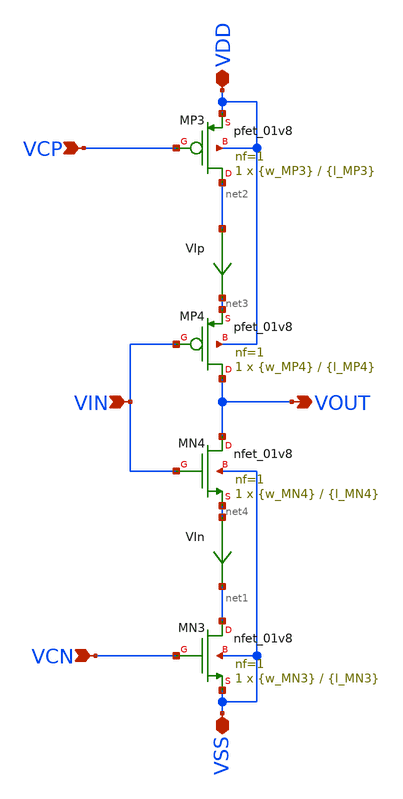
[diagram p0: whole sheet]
** sch_path: xschem/VCO/stage_starved.sch
**.subckt stage_starved VIN VOUT VDD VSS VCP VCN
*.ipin VIN
*.opin VOUT
*.iopin VDD
*.iopin VSS
*.ipin VCP
*.ipin VCN
XMP3 net2 VCP VDD VDD sky130_fd_pr__pfet_01v8 L={l_MP3} W={w_MP3} nf=1 ad='int((nf+1)/2) * W/nf * 0.29'
+ as='int((nf+2)/2) * W/nf * 0.29' pd='2*int((nf+1)/2) * (W/nf + 0.29)' ps='2*int((nf+2)/2) * (W/nf + 0.29)'
+ nrd='0.29 / W' nrs='0.29 / W' sa=0 sb=0 sd=0 mult=1 m=1
XMP4 VOUT VIN net3 VDD sky130_fd_pr__pfet_01v8 L={l_MP4} W={w_MP4} nf=1 ad='int((nf+1)/2) * W/nf * 0.29'
+ as='int((nf+2)/2) * W/nf * 0.29' pd='2*int((nf+1)/2) * (W/nf + 0.29)' ps='2*int((nf+2)/2) * (W/nf + 0.29)'
+ nrd='0.29 / W' nrs='0.29 / W' sa=0 sb=0 sd=0 mult=1 m=1
XMN4 VOUT VIN net4 VSS sky130_fd_pr__nfet_01v8 L={l_MN4} W={w_MN4} nf=1 ad='int((nf+1)/2) * W/nf * 0.29'
+ as='int((nf+2)/2) * W/nf * 0.29' pd='2*int((nf+1)/2) * (W/nf + 0.29)' ps='2*int((nf+2)/2) * (W/nf + 0.29)'
+ nrd='0.29 / W' nrs='0.29 / W' sa=0 sb=0 sd=0 mult=1 m=1
VIp net2 net3 0
.save i(vip)
VIn net4 net1 0
.save i(vin)
XMN3 net1 VCN VSS VSS sky130_fd_pr__nfet_01v8 L={l_MN3} W={w_MN3} nf=1 ad='int((nf+1)/2) * W/nf * 0.29'
+ as='int((nf+2)/2) * W/nf * 0.29' pd='2*int((nf+1)/2) * (W/nf + 0.29)' ps='2*int((nf+2)/2) * (W/nf + 0.29)'
+ nrd='0.29 / W' nrs='0.29 / W' sa=0 sb=0 sd=0 mult=1 m=1
**.ends
.end
